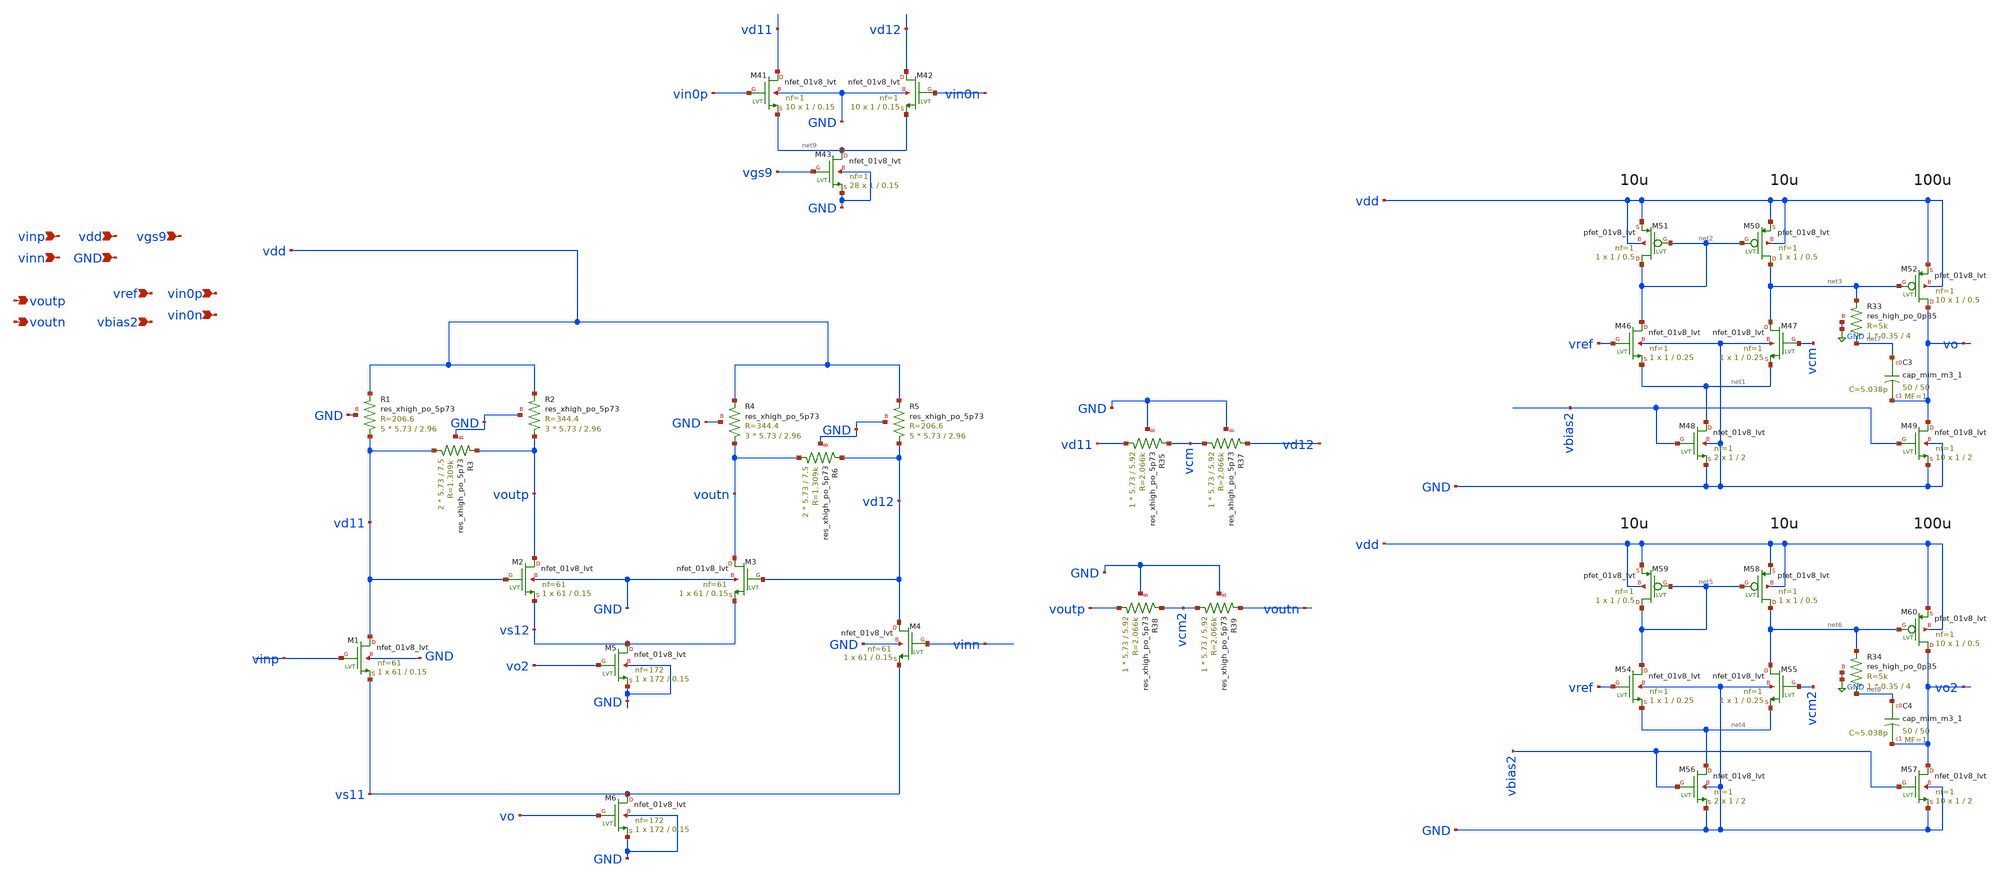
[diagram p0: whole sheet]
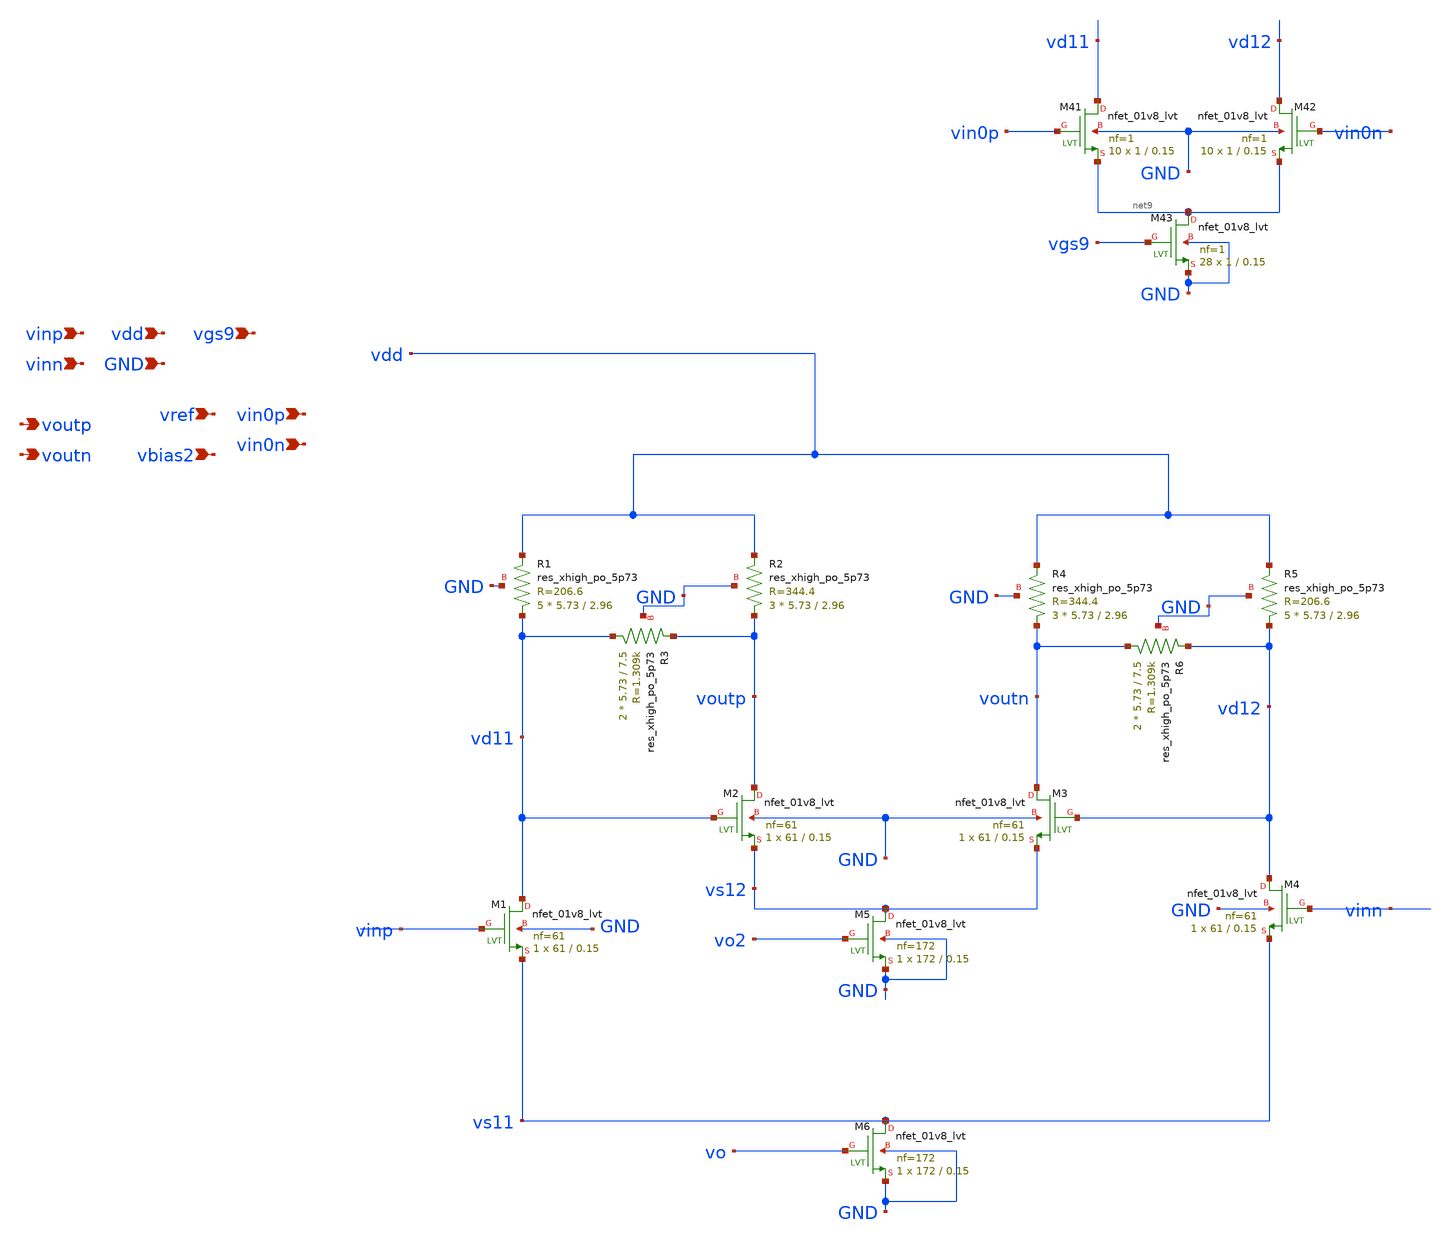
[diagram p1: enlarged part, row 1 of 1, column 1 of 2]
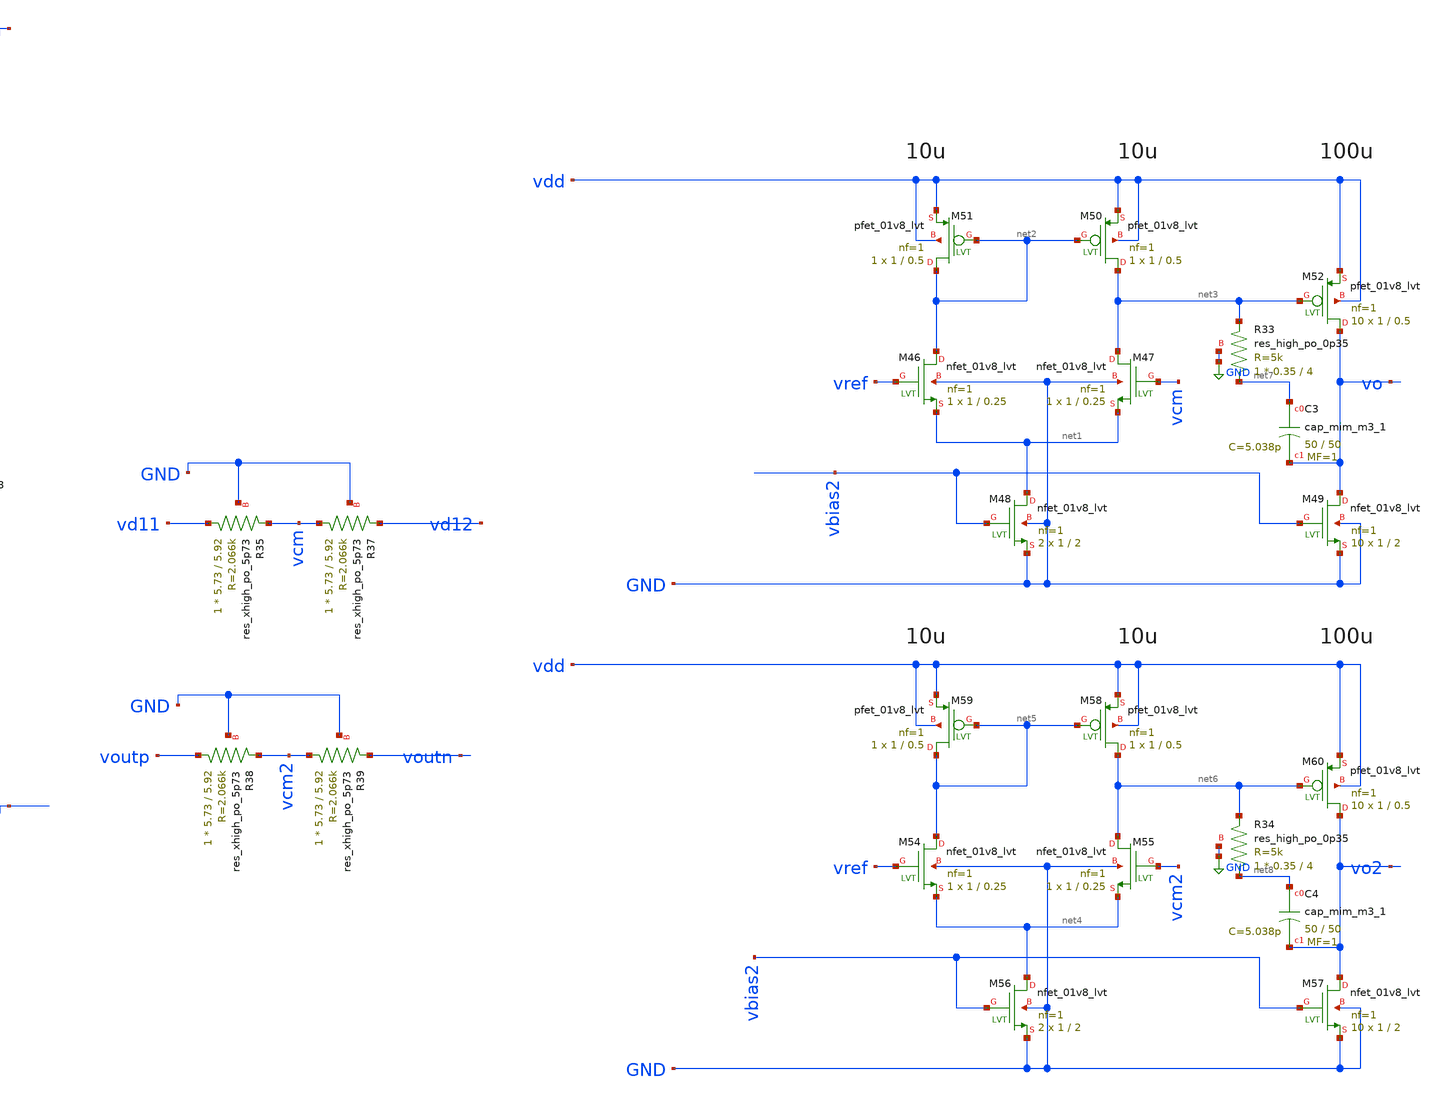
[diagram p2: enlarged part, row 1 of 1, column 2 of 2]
** sch_path: xschem/vga/VGA_preamp.sch
**.subckt VGA_preamp vinp vinn voutp voutn vdd GND vref vbias2 vin0p vin0n vgs9
*.ipin vinp
*.ipin vinn
*.opin voutp
*.opin voutn
*.ipin vdd
*.ipin GND
*.ipin vref
*.ipin vbias2
*.ipin vin0p
*.ipin vin0n
*.ipin vgs9
XR1 vd11 vdd GND sky130_fd_pr__res_xhigh_po_5p73 L=2.96 mult=5 m=5
XR2 voutp vdd GND sky130_fd_pr__res_xhigh_po_5p73 L=2.96 mult=3 m=3
XR3 vd11 voutp GND sky130_fd_pr__res_xhigh_po_5p73 L=7.5 mult=2 m=2
XR4 voutn vdd GND sky130_fd_pr__res_xhigh_po_5p73 L=2.96 mult=3 m=3
XR5 vd12 vdd GND sky130_fd_pr__res_xhigh_po_5p73 L=2.96 mult=5 m=5
XR6 voutn vd12 GND sky130_fd_pr__res_xhigh_po_5p73 L=7.5 mult=2 m=2
XM1 vd11 vinp vs11 GND sky130_fd_pr__nfet_01v8_lvt L=0.15 W=61 nf=61 ad='int((nf+1)/2) * W/nf * 0.29'
+ as='int((nf+2)/2) * W/nf * 0.29' pd='2*int((nf+1)/2) * (W/nf + 0.29)' ps='2*int((nf+2)/2) * (W/nf + 0.29)'
+ nrd='0.29 / W' nrs='0.29 / W' sa=0 sb=0 sd=0 mult=1 m=1
XM2 voutp vd11 vs12 GND sky130_fd_pr__nfet_01v8_lvt L=0.15 W=61 nf=61 ad='int((nf+1)/2) * W/nf * 0.29'
+ as='int((nf+2)/2) * W/nf * 0.29' pd='2*int((nf+1)/2) * (W/nf + 0.29)' ps='2*int((nf+2)/2) * (W/nf + 0.29)'
+ nrd='0.29 / W' nrs='0.29 / W' sa=0 sb=0 sd=0 mult=1 m=1
XM3 voutn vd12 vs12 GND sky130_fd_pr__nfet_01v8_lvt L=0.15 W=61 nf=61 ad='int((nf+1)/2) * W/nf * 0.29'
+ as='int((nf+2)/2) * W/nf * 0.29' pd='2*int((nf+1)/2) * (W/nf + 0.29)' ps='2*int((nf+2)/2) * (W/nf + 0.29)'
+ nrd='0.29 / W' nrs='0.29 / W' sa=0 sb=0 sd=0 mult=1 m=1
XM4 vd12 vinn vs11 GND sky130_fd_pr__nfet_01v8_lvt L=0.15 W=61 nf=61 ad='int((nf+1)/2) * W/nf * 0.29'
+ as='int((nf+2)/2) * W/nf * 0.29' pd='2*int((nf+1)/2) * (W/nf + 0.29)' ps='2*int((nf+2)/2) * (W/nf + 0.29)'
+ nrd='0.29 / W' nrs='0.29 / W' sa=0 sb=0 sd=0 mult=1 m=1
XM5 vs12 vo2 GND GND sky130_fd_pr__nfet_01v8_lvt L=0.15 W=172 nf=172 ad='int((nf+1)/2) * W/nf * 0.29'
+ as='int((nf+2)/2) * W/nf * 0.29' pd='2*int((nf+1)/2) * (W/nf + 0.29)' ps='2*int((nf+2)/2) * (W/nf + 0.29)'
+ nrd='0.29 / W' nrs='0.29 / W' sa=0 sb=0 sd=0 mult=1 m=1
XM6 vs11 vo GND GND sky130_fd_pr__nfet_01v8_lvt L=0.15 W=172 nf=172 ad='int((nf+1)/2) * W/nf * 0.29'
+ as='int((nf+2)/2) * W/nf * 0.29' pd='2*int((nf+1)/2) * (W/nf + 0.29)' ps='2*int((nf+2)/2) * (W/nf + 0.29)'
+ nrd='0.29 / W' nrs='0.29 / W' sa=0 sb=0 sd=0 mult=1 m=1
XM46 net2 vref net1 GND sky130_fd_pr__nfet_01v8_lvt L=0.25 W=1 nf=1 ad='int((nf+1)/2) * W/nf * 0.29'
+ as='int((nf+2)/2) * W/nf * 0.29' pd='2*int((nf+1)/2) * (W/nf + 0.29)' ps='2*int((nf+2)/2) * (W/nf + 0.29)'
+ nrd='0.29 / W' nrs='0.29 / W' sa=0 sb=0 sd=0 mult=1 m=1
XM47 net3 vcm net1 GND sky130_fd_pr__nfet_01v8_lvt L=0.25 W=1 nf=1 ad='int((nf+1)/2) * W/nf * 0.29' as='int((nf+2)/2) * W/nf * 0.29'
+ pd='2*int((nf+1)/2) * (W/nf + 0.29)' ps='2*int((nf+2)/2) * (W/nf + 0.29)' nrd='0.29 / W' nrs='0.29 / W'
+ sa=0 sb=0 sd=0 mult=1 m=1
XM48 net1 vbias2 GND GND sky130_fd_pr__nfet_01v8_lvt L=2 W=1 nf=1 ad='int((nf+1)/2) * W/nf * 0.29' as='int((nf+2)/2) * W/nf * 0.29'
+ pd='2*int((nf+1)/2) * (W/nf + 0.29)' ps='2*int((nf+2)/2) * (W/nf + 0.29)' nrd='0.29 / W' nrs='0.29 / W'
+ sa=0 sb=0 sd=0 mult=2 m=2
XM49 vo vbias2 GND GND sky130_fd_pr__nfet_01v8_lvt L=2 W=1 nf=1 ad='int((nf+1)/2) * W/nf * 0.29' as='int((nf+2)/2) * W/nf * 0.29'
+ pd='2*int((nf+1)/2) * (W/nf + 0.29)' ps='2*int((nf+2)/2) * (W/nf + 0.29)' nrd='0.29 / W' nrs='0.29 / W'
+ sa=0 sb=0 sd=0 mult=10 m=10
XM50 net3 net2 vdd vdd sky130_fd_pr__pfet_01v8_lvt L=0.5 W=1 nf=1 ad='int((nf+1)/2) * W/nf * 0.29' as='int((nf+2)/2) * W/nf * 0.29'
+ pd='2*int((nf+1)/2) * (W/nf + 0.29)' ps='2*int((nf+2)/2) * (W/nf + 0.29)' nrd='0.29 / W' nrs='0.29 / W'
+ sa=0 sb=0 sd=0 mult=1 m=1
XM51 net2 net2 vdd vdd sky130_fd_pr__pfet_01v8_lvt L=0.5 W=1 nf=1 ad='int((nf+1)/2) * W/nf * 0.29' as='int((nf+2)/2) * W/nf * 0.29'
+ pd='2*int((nf+1)/2) * (W/nf + 0.29)' ps='2*int((nf+2)/2) * (W/nf + 0.29)' nrd='0.29 / W' nrs='0.29 / W'
+ sa=0 sb=0 sd=0 mult=1 m=1
XM52 vo net3 vdd vdd sky130_fd_pr__pfet_01v8_lvt L=0.5 W=1 nf=1 ad='int((nf+1)/2) * W/nf * 0.29' as='int((nf+2)/2) * W/nf * 0.29'
+ pd='2*int((nf+1)/2) * (W/nf + 0.29)' ps='2*int((nf+2)/2) * (W/nf + 0.29)' nrd='0.29 / W' nrs='0.29 / W'
+ sa=0 sb=0 sd=0 mult=10 m=10
XC3 net7 vo sky130_fd_pr__cap_mim_m3_1 W=50 L=50 MF=1 m=1
XM54 net5 vref net4 GND sky130_fd_pr__nfet_01v8_lvt L=0.25 W=1 nf=1 ad='int((nf+1)/2) * W/nf * 0.29'
+ as='int((nf+2)/2) * W/nf * 0.29' pd='2*int((nf+1)/2) * (W/nf + 0.29)' ps='2*int((nf+2)/2) * (W/nf + 0.29)'
+ nrd='0.29 / W' nrs='0.29 / W' sa=0 sb=0 sd=0 mult=1 m=1
XM55 net6 vcm2 net4 GND sky130_fd_pr__nfet_01v8_lvt L=0.25 W=1 nf=1 ad='int((nf+1)/2) * W/nf * 0.29'
+ as='int((nf+2)/2) * W/nf * 0.29' pd='2*int((nf+1)/2) * (W/nf + 0.29)' ps='2*int((nf+2)/2) * (W/nf + 0.29)'
+ nrd='0.29 / W' nrs='0.29 / W' sa=0 sb=0 sd=0 mult=1 m=1
XM56 net4 vbias2 GND GND sky130_fd_pr__nfet_01v8_lvt L=2 W=1 nf=1 ad='int((nf+1)/2) * W/nf * 0.29' as='int((nf+2)/2) * W/nf * 0.29'
+ pd='2*int((nf+1)/2) * (W/nf + 0.29)' ps='2*int((nf+2)/2) * (W/nf + 0.29)' nrd='0.29 / W' nrs='0.29 / W'
+ sa=0 sb=0 sd=0 mult=2 m=2
XM57 vo2 vbias2 GND GND sky130_fd_pr__nfet_01v8_lvt L=2 W=1 nf=1 ad='int((nf+1)/2) * W/nf * 0.29' as='int((nf+2)/2) * W/nf * 0.29'
+ pd='2*int((nf+1)/2) * (W/nf + 0.29)' ps='2*int((nf+2)/2) * (W/nf + 0.29)' nrd='0.29 / W' nrs='0.29 / W'
+ sa=0 sb=0 sd=0 mult=10 m=10
XM58 net6 net5 vdd vdd sky130_fd_pr__pfet_01v8_lvt L=0.5 W=1 nf=1 ad='int((nf+1)/2) * W/nf * 0.29' as='int((nf+2)/2) * W/nf * 0.29'
+ pd='2*int((nf+1)/2) * (W/nf + 0.29)' ps='2*int((nf+2)/2) * (W/nf + 0.29)' nrd='0.29 / W' nrs='0.29 / W'
+ sa=0 sb=0 sd=0 mult=1 m=1
XM59 net5 net5 vdd vdd sky130_fd_pr__pfet_01v8_lvt L=0.5 W=1 nf=1 ad='int((nf+1)/2) * W/nf * 0.29' as='int((nf+2)/2) * W/nf * 0.29'
+ pd='2*int((nf+1)/2) * (W/nf + 0.29)' ps='2*int((nf+2)/2) * (W/nf + 0.29)' nrd='0.29 / W' nrs='0.29 / W'
+ sa=0 sb=0 sd=0 mult=1 m=1
XM60 vo2 net6 vdd vdd sky130_fd_pr__pfet_01v8_lvt L=0.5 W=1 nf=1 ad='int((nf+1)/2) * W/nf * 0.29' as='int((nf+2)/2) * W/nf * 0.29'
+ pd='2*int((nf+1)/2) * (W/nf + 0.29)' ps='2*int((nf+2)/2) * (W/nf + 0.29)' nrd='0.29 / W' nrs='0.29 / W'
+ sa=0 sb=0 sd=0 mult=10 m=10
XC4 net8 vo2 sky130_fd_pr__cap_mim_m3_1 W=50 L=50 MF=1 m=1
XR33 net7 net3 GND sky130_fd_pr__res_high_po_0p35 L=4 mult=1 m=1
XR34 net8 net6 GND sky130_fd_pr__res_high_po_0p35 L=4 mult=1 m=1
XR35 vd11 vcm GND sky130_fd_pr__res_xhigh_po_5p73 L=5.92 mult=1 m=1
XR37 vcm vd12 GND sky130_fd_pr__res_xhigh_po_5p73 L=5.92 mult=1 m=1
XR38 voutp vcm2 GND sky130_fd_pr__res_xhigh_po_5p73 L=5.92 mult=1 m=1
XR39 vcm2 voutn GND sky130_fd_pr__res_xhigh_po_5p73 L=5.92 mult=1 m=1
XM41 vd11 vin0p net9 GND sky130_fd_pr__nfet_01v8_lvt L=0.15 W=1 nf=1 ad='int((nf+1)/2) * W/nf * 0.29'
+ as='int((nf+2)/2) * W/nf * 0.29' pd='2*int((nf+1)/2) * (W/nf + 0.29)' ps='2*int((nf+2)/2) * (W/nf + 0.29)'
+ nrd='0.29 / W' nrs='0.29 / W' sa=0 sb=0 sd=0 mult=10 m=10
XM42 vd12 vin0n net9 GND sky130_fd_pr__nfet_01v8_lvt L=0.15 W=1 nf=1 ad='int((nf+1)/2) * W/nf * 0.29'
+ as='int((nf+2)/2) * W/nf * 0.29' pd='2*int((nf+1)/2) * (W/nf + 0.29)' ps='2*int((nf+2)/2) * (W/nf + 0.29)'
+ nrd='0.29 / W' nrs='0.29 / W' sa=0 sb=0 sd=0 mult=10 m=10
XM43 net9 vgs9 GND GND sky130_fd_pr__nfet_01v8_lvt L=0.15 W=1 nf=1 ad='int((nf+1)/2) * W/nf * 0.29' as='int((nf+2)/2) * W/nf * 0.29'
+ pd='2*int((nf+1)/2) * (W/nf + 0.29)' ps='2*int((nf+2)/2) * (W/nf + 0.29)' nrd='0.29 / W' nrs='0.29 / W'
+ sa=0 sb=0 sd=0 mult=28 m=28
**.ends
.GLOBAL GND
.end
